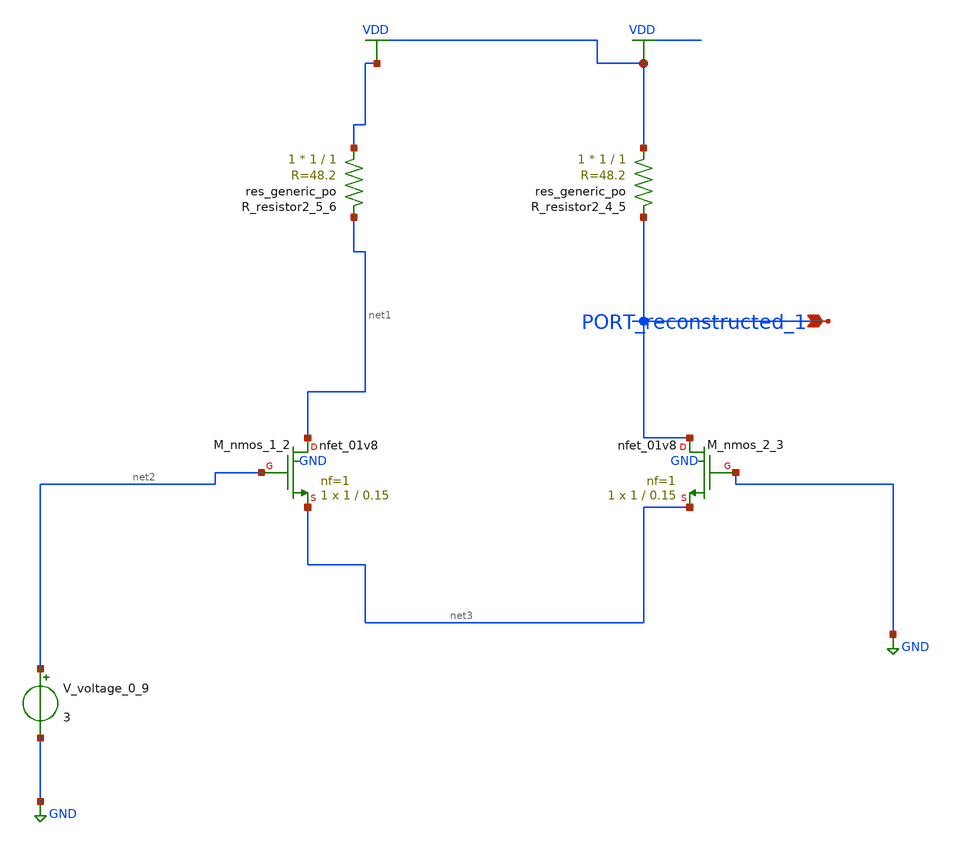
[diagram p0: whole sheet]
** sch_path: schematics/AMSNet/199.sch
**.subckt 199 PORT_reconstructed_1
*.ipin PORT_reconstructed_1
XM_nmos_1_2 net1 net2 net3 GND sky130_fd_pr__nfet_01v8 L=0.15 W=1 nf=1 ad='int((1 + 1)/2) * 1 / 1 * 0.29'
+ as='int((1 + 2)/2) * 1 / 1 * 0.29' pd='2*int((1 + 1)/2) * (1 / 1 + 0.29)' ps='2*int((1 + 2)/2) * (1 / 1 + 0.29)'
+ nrd='0.29 / 1 ' nrs='0.29 / 1 ' sa=0 sb=0 sd=0 mult=1 m=1
XM_nmos_2_3 PORT_reconstructed_1 GND net3 GND sky130_fd_pr__nfet_01v8 L=0.15 W=1 nf=1 ad='int((1 + 1)/2) * 1 / 1 * 0.29'
+ as='int((1 + 2)/2) * 1 / 1 * 0.29' pd='2*int((1 + 1)/2) * (1 / 1 + 0.29)' ps='2*int((1 + 2)/2) * (1 / 1 + 0.29)'
+ nrd='0.29 / 1 ' nrs='0.29 / 1 ' sa=0 sb=0 sd=0 mult=1 m=1
XR_resistor2_4_5 VDD PORT_reconstructed_1 sky130_fd_pr__res_generic_po W=1 L=1 m=1
XR_resistor2_5_6 VDD net1 sky130_fd_pr__res_generic_po W=1 L=1 m=1
V_voltage_0_9 net2 GND 3
**.ends
.GLOBAL GND
.GLOBAL VDD
.end
